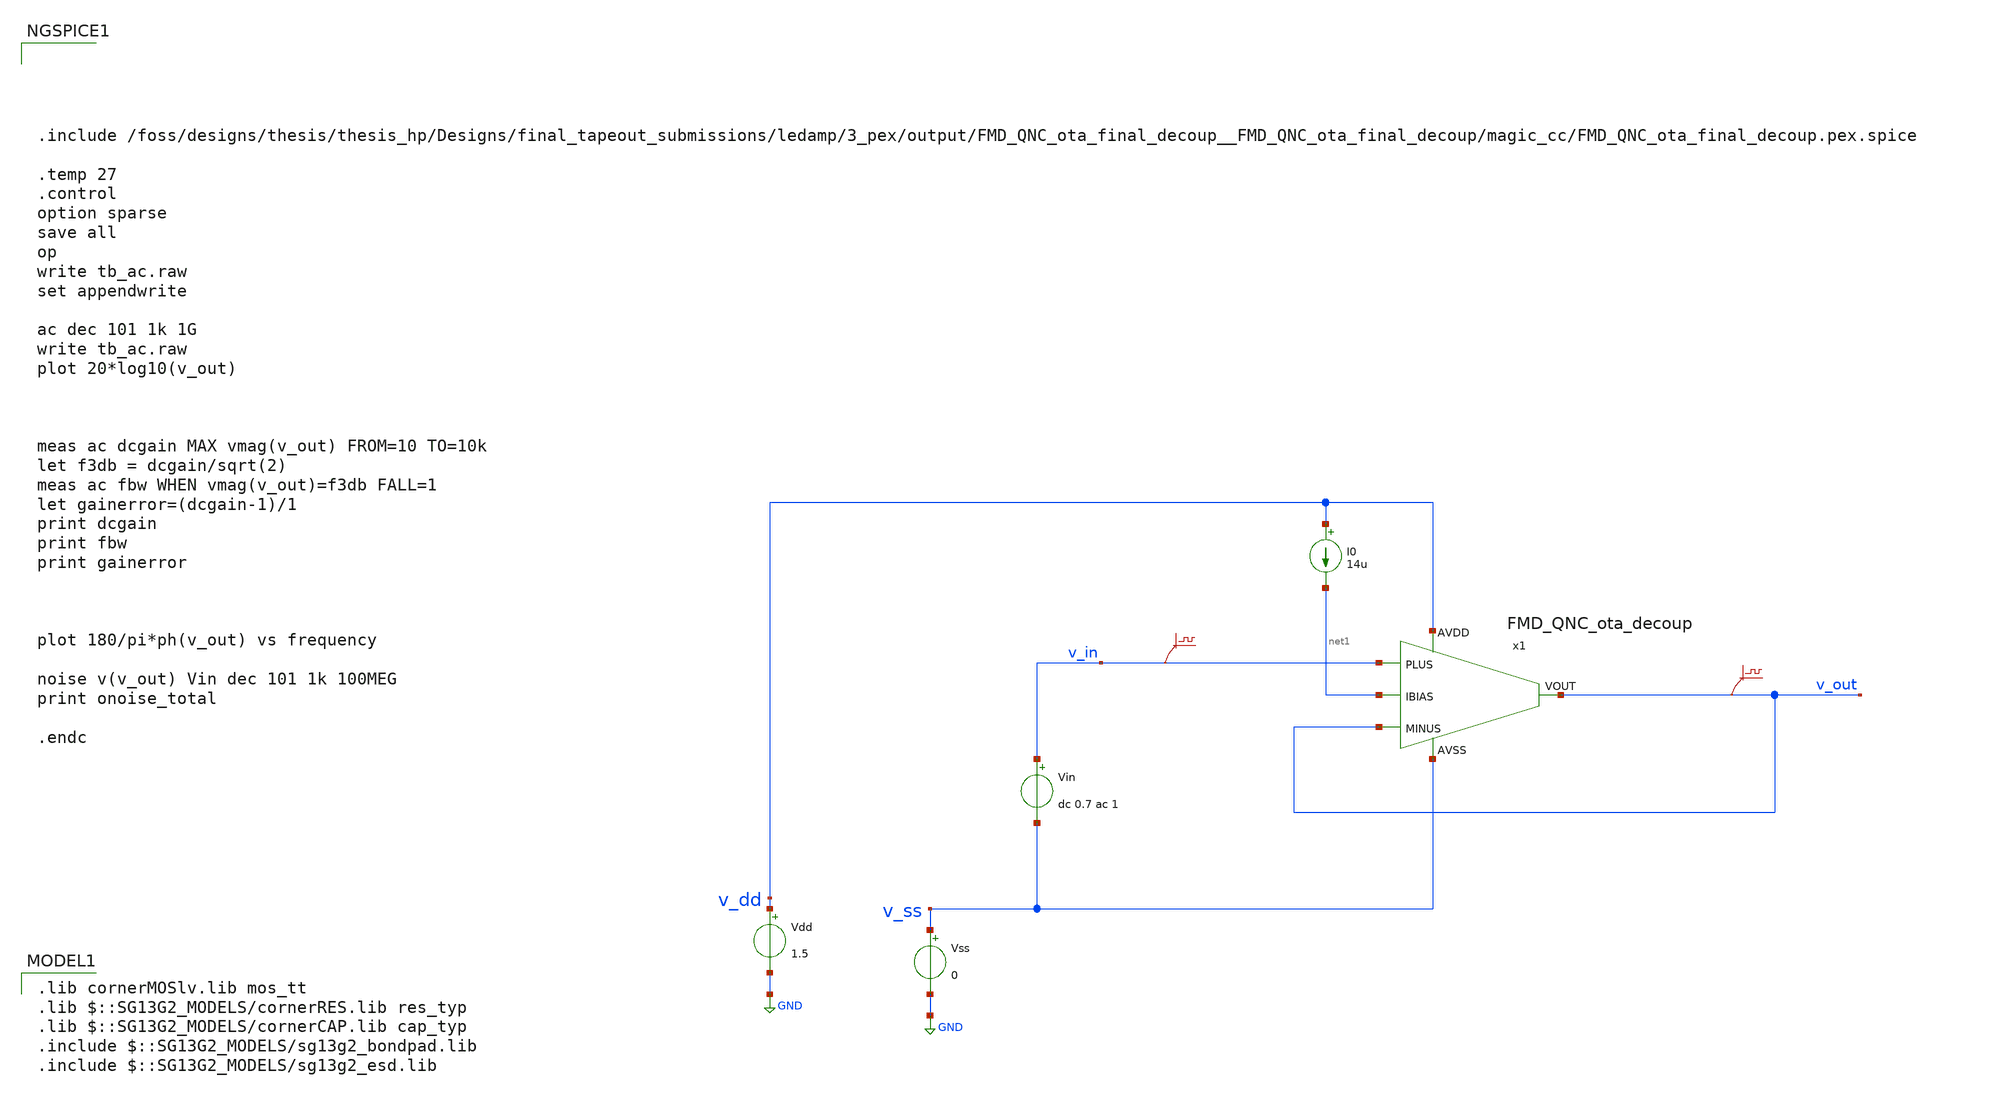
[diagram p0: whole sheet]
** sch_path: Designs/final_tapeout_submissions/ledamp/3_pex/postPEX_simulations/tb_ac.sch
* (c) 2025 Thesis_HP, Apache-2.0 license
**.subckt tb_ac
Vss v_ss GND 0
Vdd v_dd GND 1.5
Vin v_in v_ss dc 0.7 ac 1
.save v(v_in)
I0 v_dd net1 14u
.save v(v_out)
x1 v_dd net1 v_out v_out v_in v_ss FMD_QNC_ota_decoup
**** begin user architecture code





.include /foss/designs/thesis/thesis_hp/Designs/final_tapeout_submissions/ledamp/3_pex/output/FMD_QNC_ota_final_decoup__FMD_QNC_ota_final_decoup/magic_cc/FMD_QNC_ota_final_decoup.pex.spice

.temp 27
.control
option sparse
save all
op
write tb_ac.raw
set appendwrite

ac dec 101 1k 1G
write tb_ac.raw
plot 20*log10(v_out)



meas ac dcgain MAX vmag(v_out) FROM=10 TO=10k
let f3db = dcgain/sqrt(2)
meas ac fbw WHEN vmag(v_out)=f3db FALL=1
let gainerror=(dcgain-1)/1
print dcgain
print fbw
print gainerror



plot 180/pi*ph(v_out) vs frequency

noise v(v_out) Vin dec 101 1k 100MEG
print onoise_total

.endc


 .lib cornerMOSlv.lib mos_tt
.lib $::SG13G2_MODELS/cornerRES.lib res_typ
.lib $::SG13G2_MODELS/cornerCAP.lib cap_typ
.include $::SG13G2_MODELS/sg13g2_bondpad.lib
.include $::SG13G2_MODELS/sg13g2_esd.lib

**** end user architecture code
**.ends

* expanding   symbol:
*+  /foss/designs/thesis/thesis_hp/Designs/final_tapeout_submissions/ledamp/1_schematics/FMD_QNC_ota_decoup.sym # of pins=6
** sym_path: /foss/designs/thesis/thesis_hp/Designs/final_tapeout_submissions/ledamp/1_schematics/FMD_QNC_ota_decoup.sym
** sch_path: /foss/designs/thesis/thesis_hp/Designs/final_tapeout_submissions/ledamp/1_schematics/FMD_QNC_ota_decoup.sch
.subckt FMD_QNC_ota_decoup AVDD IBIAS VOUT MINUS PLUS AVSS
*.ipin PLUS
*.ipin MINUS
*.opin VOUT
*.ipin AVSS
*.ipin IBIAS
*.ipin AVDD
XM23 IBIAS IBIAS AVSS AVSS sg13_lv_nmos w=8.5u l=5u ng=4 m=1 mm_ok=1
XM24 net7 IBIAS AVSS AVSS sg13_lv_nmos w=8.5u l=5u ng=4 m=1 mm_ok=1
XM11 net7 net2 net1 AVDD sg13_lv_pmos w=14u l=2u ng=4 m=1 mm_ok=1
XM12 net1 net1 AVDD AVDD sg13_lv_pmos w=14u l=2u ng=4 m=1 mm_ok=1
XM18 AVSS net2 net5 AVDD sg13_lv_pmos w=14u l=0.5u ng=4 m=1 mm_ok=1
XM17 net5 net1 AVDD AVDD sg13_lv_pmos w=14u l=2u ng=4 m=1 mm_ok=1
XM9 net4 net1 AVDD AVDD sg13_lv_pmos w=14u l=2u ng=4 m=1 mm_ok=1
XM5 net2 net5 net4 AVDD sg13_lv_pmos w=14u l=2u ng=4 m=1 mm_ok=1
XM7 net2 net12 net3 AVSS sg13_lv_nmos w=3u l=2u ng=2 m=1 mm_ok=1
XM3 net3 net2 AVSS AVSS sg13_lv_nmos w=3u l=2u ng=2 m=1 mm_ok=1
XM30 net6 IBIAS AVSS AVSS sg13_lv_nmos w=8.5u l=5u ng=4 m=1 mm_ok=1
XM1 net4 PLUS net6 AVSS sg13_lv_nmos w=6u l=1u ng=2 m=1 mm_ok=1
XM2 net8 MINUS net6 AVSS sg13_lv_nmos w=6u l=1u ng=2 m=1 mm_ok=1
XM37 net8 AVSS AVSS AVSS sg13_lv_nmos w=6u l=1u ng=2 m=1 mm_ok=1
XM6 VOUT net5 net8 AVDD sg13_lv_pmos w=14u l=2u ng=4 m=1 mm_ok=1
XM0 net8 net1 AVDD AVDD sg13_lv_pmos w=14u l=2u ng=4 m=1 mm_ok=1
XM8 VOUT net12 net9 AVSS sg13_lv_nmos w=3u l=2u ng=2 m=1 mm_ok=1
XM4 net9 net2 AVSS AVSS sg13_lv_nmos w=3u l=2u ng=2 m=1 mm_ok=1
XM29 net9 AVSS AVSS AVSS sg13_lv_nmos w=3u l=2u ng=2 m=1 mm_ok=1
XM28 VOUT AVSS AVSS AVSS sg13_lv_nmos w=3u l=2u ng=2 m=1 mm_ok=1
XM32 net8 AVDD AVDD AVDD sg13_lv_pmos w=14u l=2u ng=4 m=1 mm_ok=1
XM33 VOUT AVDD AVDD AVDD sg13_lv_pmos w=7u l=2u ng=2 m=1 mm_ok=1
XM13 net10 net1 AVDD AVDD sg13_lv_pmos w=14u l=2u ng=4 m=1 mm_ok=1
XM15 net10 VOUT net11 AVSS sg13_lv_nmos w=3u l=2u ng=2 m=1 mm_ok=1
XM16 net11 net11 AVSS AVSS sg13_lv_nmos w=3u l=2u ng=2 m=1 mm_ok=1
XM14 net12 net11 AVSS AVSS sg13_lv_nmos w=3u l=2u ng=2 m=1 mm_ok=1
XM10 AVDD VOUT net12 AVSS sg13_lv_nmos w=15u l=0.5u ng=4 m=1 mm_ok=1
XM36 net4 AVSS AVSS AVSS sg13_lv_nmos w=6u l=1u ng=2 m=1 mm_ok=1
XM34 net2 AVDD AVDD AVDD sg13_lv_pmos w=7u l=2u ng=2 m=1 mm_ok=1
XM27 net3 AVSS AVSS AVSS sg13_lv_nmos w=3u l=2u ng=2 m=1 mm_ok=1
XM26 net2 AVSS AVSS AVSS sg13_lv_nmos w=3u l=2u ng=2 m=1 mm_ok=1
XM35 net1 AVDD AVDD AVDD sg13_lv_pmos w=7u l=2u ng=2 m=1 mm_ok=1
XM31 net11 AVSS AVSS AVSS sg13_lv_nmos w=3u l=2u ng=2 m=1 mm_ok=1
XC2 VOUT AVSS cap_cmim w=25.82e-6 l=25.82e-6 m=1 mm_ok=1
XM19 AVSS net12 AVSS AVSS sg13_lv_nmos w=8u l=1u ng=4 m=1 mm_ok=1
XM20 AVSS IBIAS AVSS AVSS sg13_lv_nmos w=8u l=1u ng=4 m=1 mm_ok=1
XM21 AVDD net1 AVDD AVDD sg13_lv_pmos w=12u l=0.5u ng=4 m=1 mm_ok=1
XM22 AVDD net5 AVDD AVDD sg13_lv_pmos w=12u l=0.5u ng=4 m=1 mm_ok=1
XD3 AVDD AVDD AVSS diodevdd_2kv m=1
XD4 AVDD AVDD AVSS diodevss_2kv m=1
XD5 AVDD AVSS net13 diodevdd_2kv m=1
XD6 AVDD AVSS net13 diodevss_2kv m=1
XX2 AVSS bondpad size=80u shape=0 padtype=0
XX3 AVDD bondpad size=80u shape=0 padtype=0
XD7 AVDD IBIAS AVSS diodevdd_2kv m=1
XD8 AVDD IBIAS AVSS diodevss_2kv m=1
XX4 IBIAS bondpad size=80u shape=0 padtype=0
XX1 VOUT bondpad size=80u shape=0 padtype=0
XD1 AVDD VOUT AVSS diodevdd_2kv m=1
XD2 AVDD VOUT AVSS diodevss_2kv m=1
XX5 PLUS bondpad size=80u shape=0 padtype=0
XD9 AVDD MINUS AVSS diodevdd_2kv m=1
XD10 AVDD MINUS AVSS diodevss_2kv m=1
XX6 MINUS bondpad size=80u shape=0 padtype=0
XD11 AVDD PLUS AVSS diodevdd_2kv m=1
XD12 AVDD PLUS AVSS diodevss_2kv m=1
.ends

.GLOBAL GND
.end
